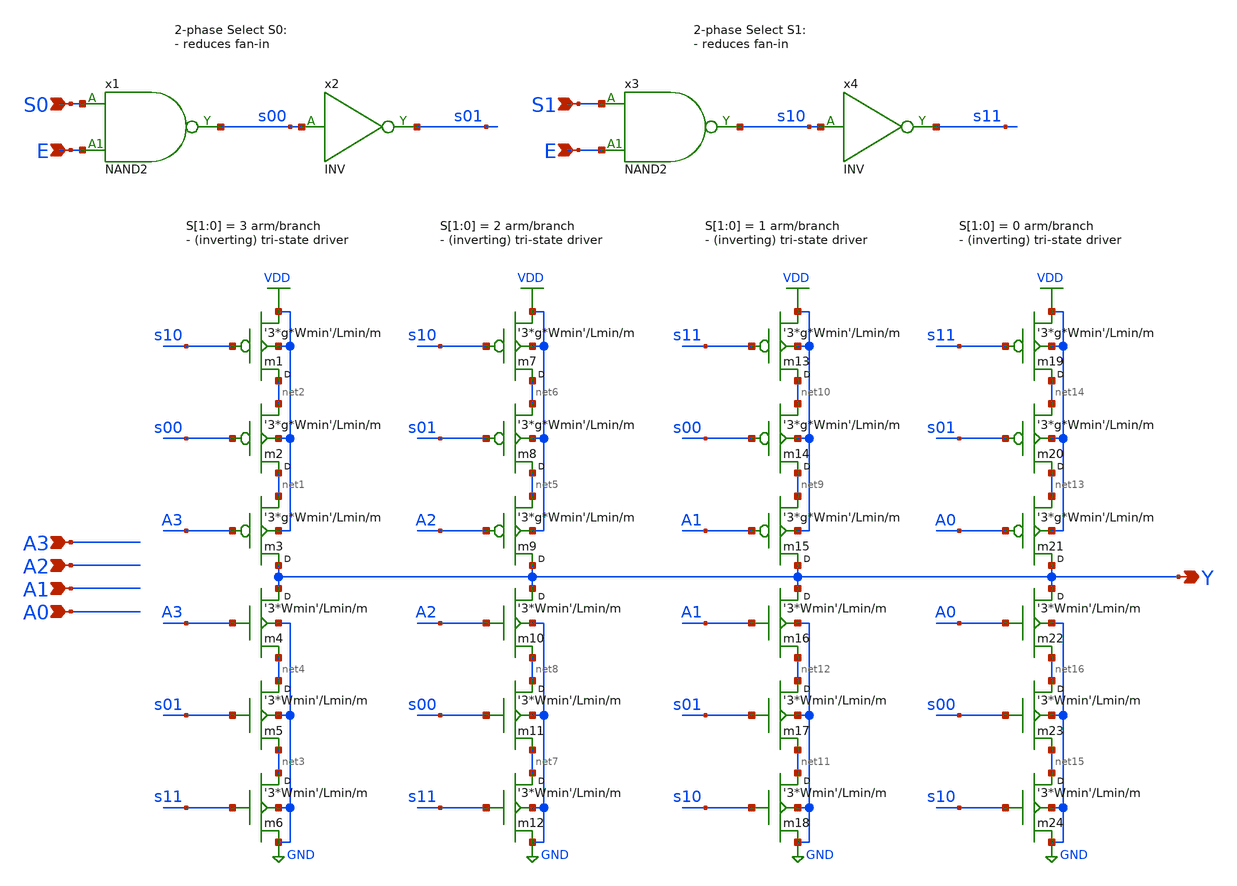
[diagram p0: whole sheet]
** sch_path: Sources/crafted/MUXIE41.sch
**.subckt MUXIE41 S0 S1 A3 Y A2 A1 A0 E E
*.ipin S0
*.ipin S1
*.ipin A3
*.opin Y
*.ipin A2
*.ipin A1
*.ipin A0
*.ipin E
*.ipin E
x2 s00 s01 VDD GND INV Wmin=1.5u Lmin=1u g=2 m=1
x4 s10 s11 VDD GND INV Wmin=1.5u Lmin=1u g=2 m=1
m4 Y A3 net4 GND nmos4 w='3*Wmin' l=Lmin m=m
m3 Y A3 net1 VDD pmos4 w='3*g*Wmin' l=Lmin m=m
m6 net3 s11 GND GND nmos4 w='3*Wmin' l=Lmin m=m
m1 net2 s10 VDD VDD pmos4 w='3*g*Wmin' l=Lmin m=m
m2 net1 s00 net2 VDD pmos4 w='3*g*Wmin' l=Lmin m=m
m5 net4 s01 net3 GND nmos4 w='3*Wmin' l=Lmin m=m
m10 Y A2 net8 GND nmos4 w='3*Wmin' l=Lmin m=m
m9 Y A2 net5 VDD pmos4 w='3*g*Wmin' l=Lmin m=m
m12 net7 s11 GND GND nmos4 w='3*Wmin' l=Lmin m=m
m7 net6 s10 VDD VDD pmos4 w='3*g*Wmin' l=Lmin m=m
m8 net5 s01 net6 VDD pmos4 w='3*g*Wmin' l=Lmin m=m
m11 net8 s00 net7 GND nmos4 w='3*Wmin' l=Lmin m=m
m16 Y A1 net12 GND nmos4 w='3*Wmin' l=Lmin m=m
m15 Y A1 net9 VDD pmos4 w='3*g*Wmin' l=Lmin m=m
m18 net11 s10 GND GND nmos4 w='3*Wmin' l=Lmin m=m
m13 net10 s11 VDD VDD pmos4 w='3*g*Wmin' l=Lmin m=m
m14 net9 s00 net10 VDD pmos4 w='3*g*Wmin' l=Lmin m=m
m17 net12 s01 net11 GND nmos4 w='3*Wmin' l=Lmin m=m
m22 Y A0 net16 GND nmos4 w='3*Wmin' l=Lmin m=m
m21 Y A0 net13 VDD pmos4 w='3*g*Wmin' l=Lmin m=m
m24 net15 s10 GND GND nmos4 w='3*Wmin' l=Lmin m=m
m19 net14 s11 VDD VDD pmos4 w='3*g*Wmin' l=Lmin m=m
m20 net13 s01 net14 VDD pmos4 w='3*g*Wmin' l=Lmin m=m
m23 net16 s00 net15 GND nmos4 w='3*Wmin' l=Lmin m=m
x1 S0 E s00 VDD GND NAND2 Wmin=1.5u Lmin=1u g=2 m=1
x3 S1 E s10 VDD GND NAND2 Wmin=1.5u Lmin=1u g=2 m=1
**.ends
.GLOBAL GND
.GLOBAL VDD
.end
